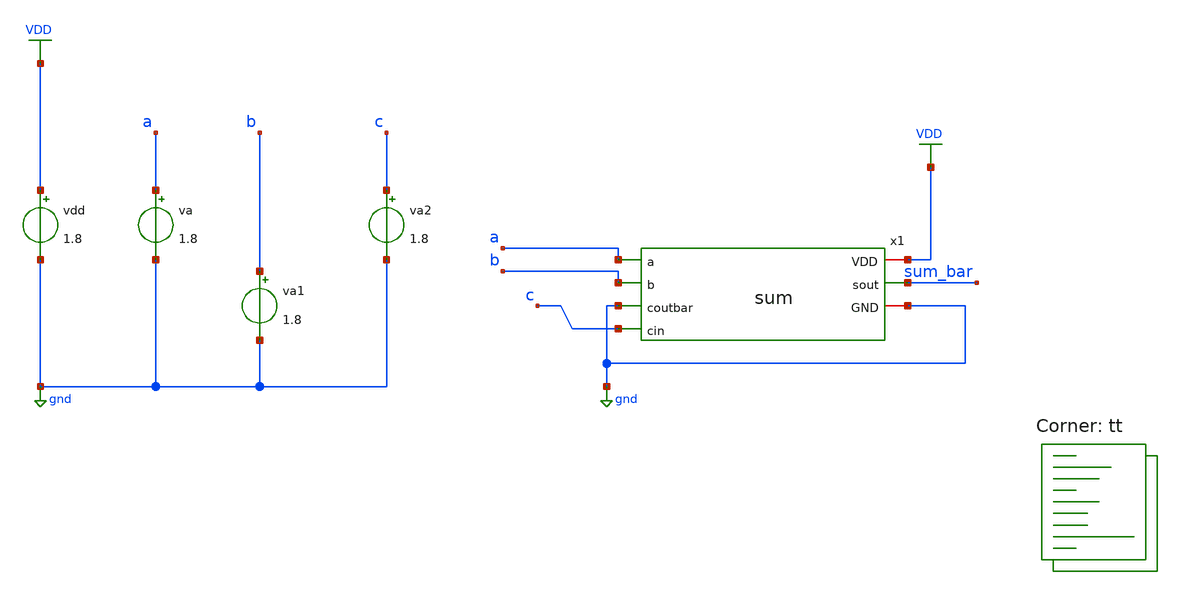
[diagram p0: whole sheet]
** sch_path: assignments/assignment7/sum_tb.sch
**.subckt sum_tb
x1 VDD a b gnd c sum_bar gnd sum
vdd VDD gnd 1.8
va a gnd 1.8
va1 b gnd 1.8
va2 c gnd 1.8
**** begin user architecture code


.include sum_extracted.spice
.control
*alter @va[pulse] = [ 1.8 0 10p 5p 5p]
*alter @va1[pulse] = [ 0 1.8 10p 5p 5p]
*alter @va2[pulse] = [ 1.8 0 10p 5p 5p]

tran 1p 400p

plot v(a) v(b) v(c) v(sum_bar)
print v(sum_bar)
.endc


.lib $::SKYWATER_MODELS/sky130.lib.spice tt
**** end user architecture code
**.ends
.GLOBAL VDD
.GLOBAL gnd
.end
